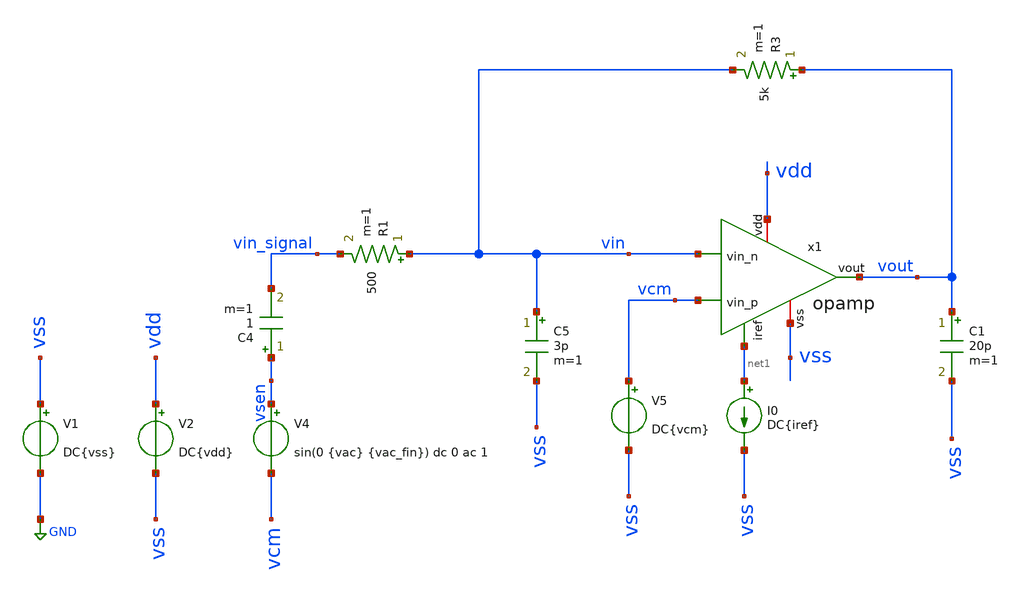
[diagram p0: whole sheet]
** sch_path: tb_opamp_closeloop.sch
**.subckt tb_opamp_closeloop
V1 vss GND DC{vss}
V2 vdd vss DC{vdd}
V4 vsen vcm sin(0 {vac} {vac_fin}) dc 0 ac 1
C4 vsen vin_signal 1 m=1
I0 net1 vss DC{iref}
R1 vin vin_signal 500 m=1
R3 vout vin 5k m=1
C5 vin vss 3p m=1
C1 vout vss 20p m=1
V5 vcm vss DC{vcm}
x1 vdd net1 vin vcm vout vss opamp
**** begin user architecture code




* Circuit Parameters
.param vss  = 0.0
.param vac  = 60m
.param w857 = 15
.param l857 = 0.9
.param m857 = 1.2
.param wpar = 30
.param lpar = 0.45
.param mpar = 15
.param w34  = 6
.param l34  = 2
.param m34  = 6
.param w6   = 20
.param l6   = 1.5
.param m6   = 15

* Corner Dependant Parameters
.param vdd    = 1.8
.param vcm    = 0.8
.param iref   = 100u
.options TEMP = 65.0

* FFT Parameters
.param Ts_FFT     = 1e-9
.csparam Ts_FFT   = {Ts_FFT}
.param fin_approx = 1e6
.param NFFT       = 4096
.csparam NFFT     = {NFFT}
.param vac_fin    = 'floor(fin_approx*Ts_FFT*NFFT)/Ts_FFT/NFFT'
.csparam Ti_FFT   = 3u
.csparam vac_fin  = {vac_fin}

* Include Models
.lib ~/skywater/skywater-pdk/libraries/sky130_fd_pr_ngspice/latest/models/corners/sky130.lib SS

* OP Parameters & Singals to save
.save all  @M.X1.XM1.msky130_fd_pr__pfet_01v8_lvt[id] @M.X1.XM1.msky130_fd_pr__pfet_01v8_lvt[vth] @M.X1.XM1.msky130_fd_pr__pfet_01v8_lvt[vgs] @M.X1.XM1.msky130_fd_pr__pfet_01v8_lvt[vds] @M.X1.XM1.msky130_fd_pr__pfet_01v8_lvt[vdsat] @M.X1.XM1.msky130_fd_pr__pfet_01v8_lvt[gm] @M.X1.XM1.msky130_fd_pr__pfet_01v8_lvt[gds] @M.X1.XM1.msky130_fd_pr__pfet_01v8_lvt[cgg]  @M.X1.XM2.msky130_fd_pr__pfet_01v8_lvt[id] @M.X1.XM2.msky130_fd_pr__pfet_01v8_lvt[vth] @M.X1.XM2.msky130_fd_pr__pfet_01v8_lvt[vgs] @M.X1.XM2.msky130_fd_pr__pfet_01v8_lvt[vds] @M.X1.XM2.msky130_fd_pr__pfet_01v8_lvt[vdsat] @M.X1.XM2.msky130_fd_pr__pfet_01v8_lvt[gm] @M.X1.XM2.msky130_fd_pr__pfet_01v8_lvt[gds] @M.X1.XM2.msky130_fd_pr__pfet_01v8_lvt[cgg]  @M.X1.XM3.msky130_fd_pr__nfet_01v8[id] @M.X1.XM3.msky130_fd_pr__nfet_01v8[vth] @M.X1.XM3.msky130_fd_pr__nfet_01v8[vgs] @M.X1.XM3.msky130_fd_pr__nfet_01v8[vds] @M.X1.XM3.msky130_fd_pr__nfet_01v8[vdsat] @M.X1.XM3.msky130_fd_pr__nfet_01v8[gm] @M.X1.XM3.msky130_fd_pr__nfet_01v8[gds] @M.X1.XM3.msky130_fd_pr__nfet_01v8[cgg]  @M.X1.XM4.msky130_fd_pr__nfet_01v8[id] @M.X1.XM4.msky130_fd_pr__nfet_01v8[vth] @M.X1.XM4.msky130_fd_pr__nfet_01v8[vgs] @M.X1.XM4.msky130_fd_pr__nfet_01v8[vds] @M.X1.XM4.msky130_fd_pr__nfet_01v8[vdsat] @M.X1.XM4.msky130_fd_pr__nfet_01v8[gm] @M.X1.XM4.msky130_fd_pr__nfet_01v8[gds] @M.X1.XM4.msky130_fd_pr__nfet_01v8[cgg]  @M.X1.XM5.msky130_fd_pr__pfet_01v8[id] @M.X1.XM5.msky130_fd_pr__pfet_01v8[vth] @M.X1.XM5.msky130_fd_pr__pfet_01v8[vgs] @M.X1.XM5.msky130_fd_pr__pfet_01v8[vds] @M.X1.XM5.msky130_fd_pr__pfet_01v8[vdsat] @M.X1.XM5.msky130_fd_pr__pfet_01v8[gm] @M.X1.XM5.msky130_fd_pr__pfet_01v8[gds] @M.X1.XM5.msky130_fd_pr__pfet_01v8[cgg]  @M.X1.XM6.msky130_fd_pr__nfet_01v8[id] @M.X1.XM6.msky130_fd_pr__nfet_01v8[vth] @M.X1.XM6.msky130_fd_pr__nfet_01v8[vgs] @M.X1.XM6.msky130_fd_pr__nfet_01v8[vds] @M.X1.XM6.msky130_fd_pr__nfet_01v8[vdsat] @M.X1.XM6.msky130_fd_pr__nfet_01v8[gm] @M.X1.XM6.msky130_fd_pr__nfet_01v8[gds] @M.X1.XM6.msky130_fd_pr__nfet_01v8[cgg]  @M.X1.XM7.msky130_fd_pr__pfet_01v8[id] @M.X1.XM7.msky130_fd_pr__pfet_01v8[vth] @M.X1.XM7.msky130_fd_pr__pfet_01v8[vgs] @M.X1.XM7.msky130_fd_pr__pfet_01v8[vds] @M.X1.XM7.msky130_fd_pr__pfet_01v8[vdsat] @M.X1.XM7.msky130_fd_pr__pfet_01v8[gm] @M.X1.XM7.msky130_fd_pr__pfet_01v8[gds] @M.X1.XM7.msky130_fd_pr__pfet_01v8[cgg]  @M.X1.XM8.msky130_fd_pr__pfet_01v8[id] @M.X1.XM8.msky130_fd_pr__pfet_01v8[vth] @M.X1.XM8.msky130_fd_pr__pfet_01v8[vgs] @M.X1.XM8.msky130_fd_pr__pfet_01v8[vds] @M.X1.XM8.msky130_fd_pr__pfet_01v8[vdsat] @M.X1.XM8.msky130_fd_pr__pfet_01v8[gm] @M.X1.XM8.msky130_fd_pr__pfet_01v8[gds] @M.X1.XM8.msky130_fd_pr__pfet_01v8[cgg]  @M.X1.XM9.msky130_fd_pr__nfet_01v8[id] @M.X1.XM9.msky130_fd_pr__nfet_01v8[vth] @M.X1.XM9.msky130_fd_pr__nfet_01v8[vgs] @M.X1.XM9.msky130_fd_pr__nfet_01v8[vds] @M.X1.XM9.msky130_fd_pr__nfet_01v8[vdsat] @M.X1.XM9.msky130_fd_pr__nfet_01v8[gm] @M.X1.XM9.msky130_fd_pr__nfet_01v8[gds] @M.X1.XM9.msky130_fd_pr__nfet_01v8[cgg]

*Simulation
.control
  set color0 = white

  ac dec 100 1k 10G
  setplot ac1
  meas ac GBW when vdb(vout)=0
  meas ac DCG find vdb(vout) at=1k
  plot vdb(vout) {vp(vout)*180/PI}

  reset
  tran 0.01u 11u
  setplot tran1
  plot v(vsen) v(vout)

  *reset
  *set sqrnoise
  *noise v(vout) V4 dec 100 1k 10G 1
  *setplot noise1
  *plot onoise_spectrum
  *plot sqrt(integ(onoise_spectrum))
  *let onoise_total_integrado = maximum(sqrt(integ(onoise_spectrum)))
  *print onoise_total_integrado

  reset
  noise v(vout) V4 dec 100 1k 10G 1
  setplot noise1
  plot onoise_spectrum
  setplot noise2
  print inoise_total
  print onoise_total
  print onoise_total.m.x1.xm1.msky130_fd_pr__pfet_01v8_lvt.1overf
  print onoise_total.m.x1.xm1.msky130_fd_pr__pfet_01v8_lvt.id
  print onoise_total.m.x1.xm2.msky130_fd_pr__pfet_01v8_lvt.1overf
  print onoise_total.m.x1.xm2.msky130_fd_pr__pfet_01v8_lvt.id
  print onoise_total.m.x1.xm3.msky130_fd_pr__nfet_01v8.1overf
  print onoise_total.m.x1.xm3.msky130_fd_pr__nfet_01v8.id
  print onoise_total.m.x1.xm4.msky130_fd_pr__nfet_01v8.1overf
  print onoise_total.m.x1.xm4.msky130_fd_pr__nfet_01v8.id
  print onoise_total.m.x1.xm5.msky130_fd_pr__pfet_01v8.1overf
  print onoise_total.m.x1.xm5.msky130_fd_pr__pfet_01v8.id
  print onoise_total.m.x1.xm6.msky130_fd_pr__nfet_01v8.1overf
  print onoise_total.m.x1.xm6.msky130_fd_pr__nfet_01v8.id
  print onoise_total.m.x1.xm7.msky130_fd_pr__pfet_01v8.1overf
  print onoise_total.m.x1.xm7.msky130_fd_pr__pfet_01v8.id
  vprint onoise_total.m.x1.xm8.msky130_fd_pr__pfet_01v8.1overf
  print onoise_total.m.x1.xm8.msky130_fd_pr__pfet_01v8.id
  set filetype=ascii
  write tpfinal_noise.raw

  reset
  tran 0.001u 11u
  fourier 9.765625e5 vout
  let THD_db = db(fourier11[1][3]/fourier11[1][1])
  print THD_db
  let lin-tstart = {Ti_FFT} $ skip the start - up phase
  let lin-tstep = {Ts_FFT}
  let lin-tstop = {Ti_FFT + (NFFT-1) * Ts_FFT} $ end earlier
  linearize vout
  set specwindow = none
  fft vout
  *plot mag(vout)
  plot db(mag(vout)) xlimit 0 20e6

  reset
  op
  setplot op1
  unset filetype
  write tb_opamp_closeloop.raw

.endc

.end


**** end user architecture code
**.ends

* expanding   symbol:  opamp.sym # of pins=6
** sym_path: opamp.sym
** sch_path: opamp.sch
.subckt opamp vdd iref vin_n vin_p vout vss
*.iopin vdd
*.iopin vss
*.ipin vin_n
*.ipin vin_p
*.ipin iref
*.opin vout
XM3 vbn vbn vss vss sky130_fd_pr__nfet_01v8 L={l34} W={w34} nf=1 ad='W * 0.29' as='W * 0.29' pd='2 * (W + 0.29)'
+ ps='2 * (W + 0.29)' nrd='0.29 / W' nrs='0.29 / W' sa=0 sb=0 sd=0 mult={m34} m={m34}
XM4 voe1 vbn vss vss sky130_fd_pr__nfet_01v8 L={l34} W={w34} nf=1 ad='W * 0.29' as='W * 0.29' pd='2 * (W + 0.29)'
+ ps='2 * (W + 0.29)' nrd='0.29 / W' nrs='0.29 / W' sa=0 sb=0 sd=0 mult={m34} m={m34}
XM5 vp iref vdd vdd sky130_fd_pr__pfet_01v8 L={l857} W={w857} nf=1 ad='W * 0.29' as='W * 0.29' pd='2 * (W + 0.29)'
+ ps='2 * (W + 0.29)' nrd='0.29 / W' nrs='0.29 / W' sa=0 sb=0 sd=0 mult=20 m=20
XM7 vout iref vdd vdd sky130_fd_pr__pfet_01v8 L={l857} W={w857} nf=1 ad='W * 0.29' as='W * 0.29' pd='2 * (W + 0.29)'
+ ps='2 * (W + 0.29)' nrd='0.29 / W' nrs='0.29 / W' sa=0 sb=0 sd=0 mult=200 m=200
XM8 iref iref vdd vdd sky130_fd_pr__pfet_01v8 L={l857} W={w857} nf=1 ad='W * 0.29' as='W * 0.29' pd='2 * (W + 0.29)'
+ ps='2 * (W + 0.29)' nrd='0.29 / W' nrs='0.29 / W' sa=0 sb=0 sd=0 mult=10 m=10
XM9 net1 vdd voe1 vss sky130_fd_pr__nfet_01v8 L=0.4 W=3 nf=1 ad='W * 0.29' as='W * 0.29' pd='2 * (W + 0.29)'
+ ps='2 * (W + 0.29)' nrd='0.29 / W' nrs='0.29 / W' sa=0 sb=0 sd=0 mult=3 m=3
XM6 vout voe1 vss vss sky130_fd_pr__nfet_01v8 L={l6} W={w6} nf=1 ad='W * 0.29' as='W * 0.29' pd='2 * (W + 0.29)'
+ ps='2 * (W + 0.29)' nrd='0.29 / W' nrs='0.29 / W' sa=0 sb=0 sd=0 mult={m6} m={m6}
XM1 vbn vin_n vp vp sky130_fd_pr__pfet_01v8_lvt L={lpar} W={wpar} nf=1 ad='int((nf+1)/2) * W/nf * 0.29'
+ as='int((nf+2)/2) * W/nf * 0.29' pd='2*int((nf+1)/2) * (W/nf + 0.29)' ps='2*int((nf+2)/2) * (W/nf + 0.29)'
+ nrd='0.29 / W' nrs='0.29 / W' sa=0 sb=0 sd=0 mult={mpar} m={mpar}
XM2 voe1 vin_p vp vp sky130_fd_pr__pfet_01v8_lvt L={lpar} W={wpar} nf=1 ad='int((nf+1)/2) * W/nf * 0.29'
+ as='int((nf+2)/2) * W/nf * 0.29' pd='2*int((nf+1)/2) * (W/nf + 0.29)' ps='2*int((nf+2)/2) * (W/nf + 0.29)'
+ nrd='0.29 / W' nrs='0.29 / W' sa=0 sb=0 sd=0 mult={mpar} m={mpar}
C1 net1 vout 3.8p m=1
.ends

.GLOBAL GND
.end
